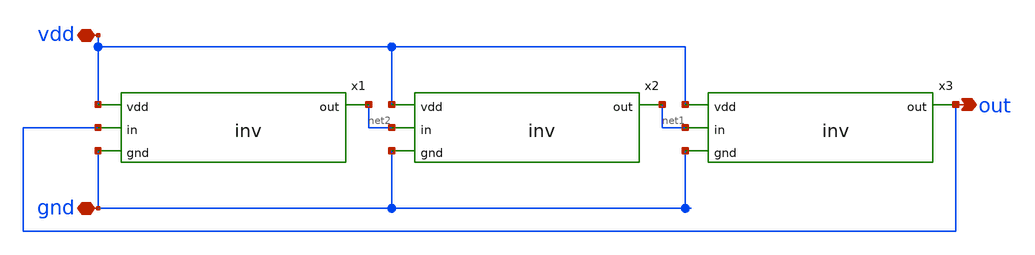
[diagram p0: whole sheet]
** sch_path: ring-osilator.sch
**.subckt ring-osilator vdd gnd out
*.iopin vdd
*.iopin gnd
*.opin out
x1 vdd out net2 gnd inv
x2 vdd net2 net1 gnd inv
x3 vdd net1 out gnd inv
**.ends

* expanding   symbol:  inv.sym # of pins=4
** sym_path: inv.sym
** sch_path: inv.sch
.subckt inv vdd in out gnd
*.ipin in
*.ipin vdd
*.ipin gnd
*.opin out
XM1 out in gnd gnd sky130_fd_pr__nfet_01v8 L=0.15 W=1 nf=1 ad='int((nf+1)/2) * W/nf * 0.29' as='int((nf+2)/2) * W/nf * 0.29'
+ pd='2*int((nf+1)/2) * (W/nf + 0.29)' ps='2*int((nf+2)/2) * (W/nf + 0.29)' nrd='0.29 / W' nrs='0.29 / W'
+ sa=0 sb=0 sd=0 mult=1 m=1
XM2 out in vdd vdd sky130_fd_pr__pfet_01v8 L=0.15 W=1 nf=1 ad='int((nf+1)/2) * W/nf * 0.29' as='int((nf+2)/2) * W/nf * 0.29'
+ pd='2*int((nf+1)/2) * (W/nf + 0.29)' ps='2*int((nf+2)/2) * (W/nf + 0.29)' nrd='0.29 / W' nrs='0.29 / W'
+ sa=0 sb=0 sd=0 mult=1 m=1
.ends

.end
